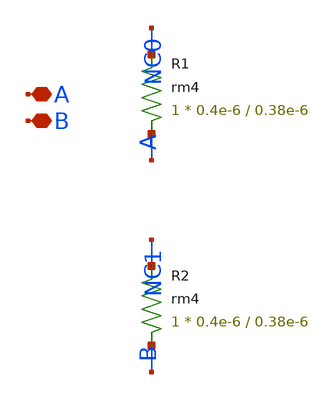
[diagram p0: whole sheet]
** sch_path: design/LELO_SAR9B_GF180MCUD/LELOSAR_CAP_BSSW_CV.sch
**.subckt LELOSAR_CAP_BSSW_CV A B
*.iopin A
*.iopin B
XR1 A NC0 rm4 r_width=0.4e-6 r_length=0.38e-6 m=1
XR2 B NC1 rm4 r_width=0.4e-6 r_length=0.38e-6 m=1
**.ends
.end
